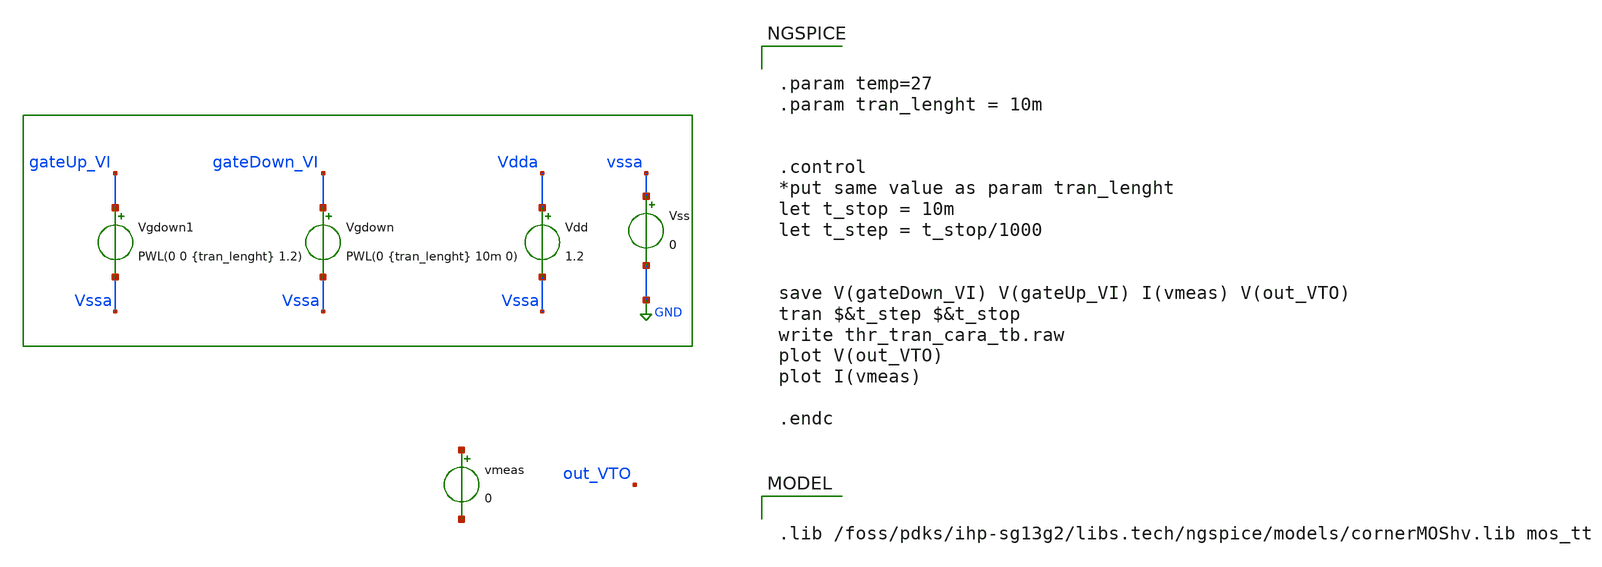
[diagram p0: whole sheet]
** sch_path: test_bench/threshold_trans_cara_tb.sch
**.subckt threshold_trans_cara_tb
Vgdown1 gateUp_VI Vssa PWL(0 0 {tran_lenght} 1.2)
Vdd Vdda Vssa 1.2
Vgdown gateDown_VI Vssa PWL(0 {tran_lenght} 10m 0)
vmeas net1 net2 0
Vss vssa GND 0
**** begin user architecture code

.lib /foss/pdks/ihp-sg13g2/libs.tech/ngspice/models/cornerMOShv.lib mos_tt



.param temp=27
.param tran_lenght = 10m


.control
*put same value as param tran_lenght
let t_stop = 10m
let t_step = t_stop/1000


save V(gateDown_VI) V(gateUp_VI) I(vmeas) V(out_VTO)
tran $&t_step $&t_stop
write thr_tran_cara_tb.raw
plot V(out_VTO)
plot I(vmeas)

.endc


**** end user architecture code
**.ends
.GLOBAL GND
.end
